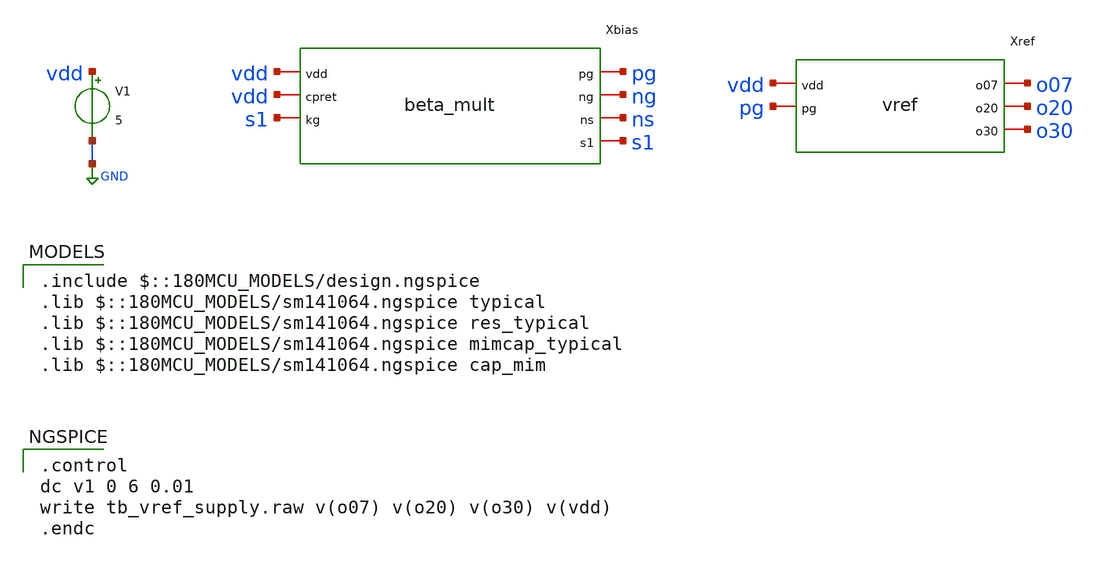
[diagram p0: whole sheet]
** sch_path: schematic pt2/sims/tb/tb_vref_supply.sch
**.subckt tb_vref_supply
V1 vdd GND 5
Xbias vdd pg ng ns vdd s1 s1 beta_mult
Xref vdd pg o07 o20 o30 vref
**** begin user architecture code
 .include $::180MCU_MODELS/design.ngspice
.lib $::180MCU_MODELS/sm141064.ngspice typical
.lib $::180MCU_MODELS/sm141064.ngspice res_typical
.lib $::180MCU_MODELS/sm141064.ngspice mimcap_typical
.lib $::180MCU_MODELS/sm141064.ngspice cap_mim

.control
dc v1 0 6 0.01
write tb_vref_supply.raw v(o07) v(o20) v(o30) v(vdd)
.endc

**** end user architecture code
**.ends
.GLOBAL GND
.end
